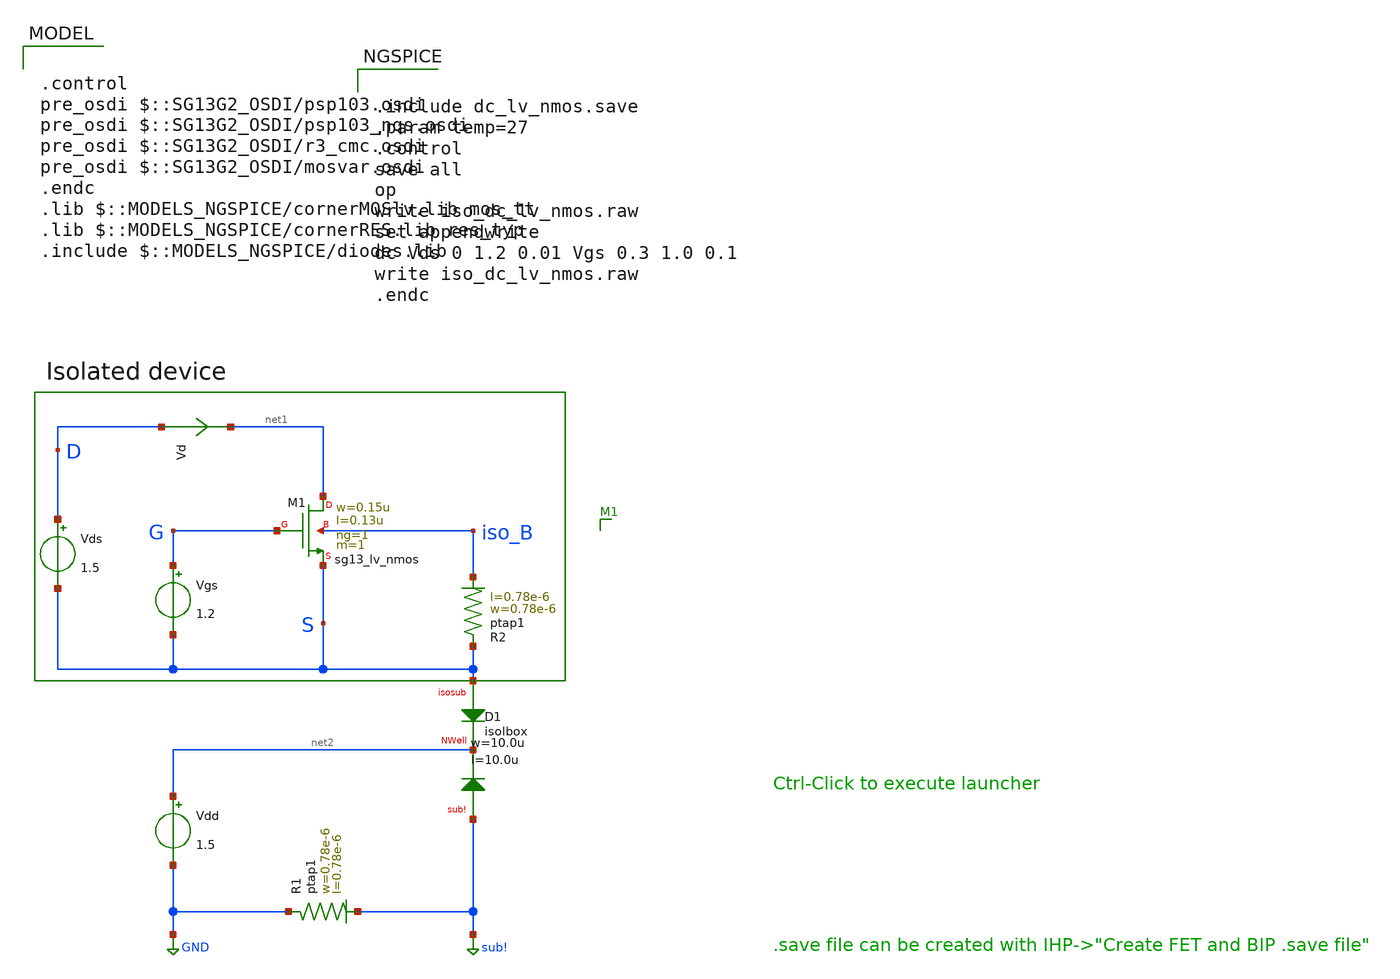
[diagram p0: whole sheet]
** sch_path: ihp-sg13g2/xschem_libs/sg13g2_tests/iso_dc_lv_nmos/schematic/iso_dc_lv_nmos.sch
* Copyright 2023 IHP PDK Authors
**.subckt iso_dc_lv_nmos
Vgs G S 1.2
Vds D S 1.5
Vd D net1 0
.save i(vd)
XM1 net1 G S iso_B sg13_lv_nmos w=0.15u l=0.13u ng=1 m=1 mm_ok=1
XD1 S net2 sub! isolbox l=10.0u w=10.0u
XR1 GND sub! ptap1 R=262.8 w=0.78e-6 l=0.78e-6
XR2 S iso_B ptap1 R=262.8 w=0.78e-6 l=0.78e-6
Vdd net2 GND 1.5
**** begin user architecture code

.control
pre_osdi $::SG13G2_OSDI/psp103.osdi
pre_osdi $::SG13G2_OSDI/psp103_nqs.osdi
pre_osdi $::SG13G2_OSDI/r3_cmc.osdi
pre_osdi $::SG13G2_OSDI/mosvar.osdi
.endc
.lib $::MODELS_NGSPICE/cornerMOSlv.lib mos_tt
.lib $::MODELS_NGSPICE/cornerRES.lib res_typ
.include $::MODELS_NGSPICE/diodes.lib



.include dc_lv_nmos.save
.param temp=27
.control
save all
op
write iso_dc_lv_nmos.raw
set appendwrite
dc Vds 0 1.2 0.01 Vgs 0.3 1.0 0.1
write iso_dc_lv_nmos.raw
.endc


**** end user architecture code
**.ends
.GLOBAL GND
.GLOBAL sub!
.end
